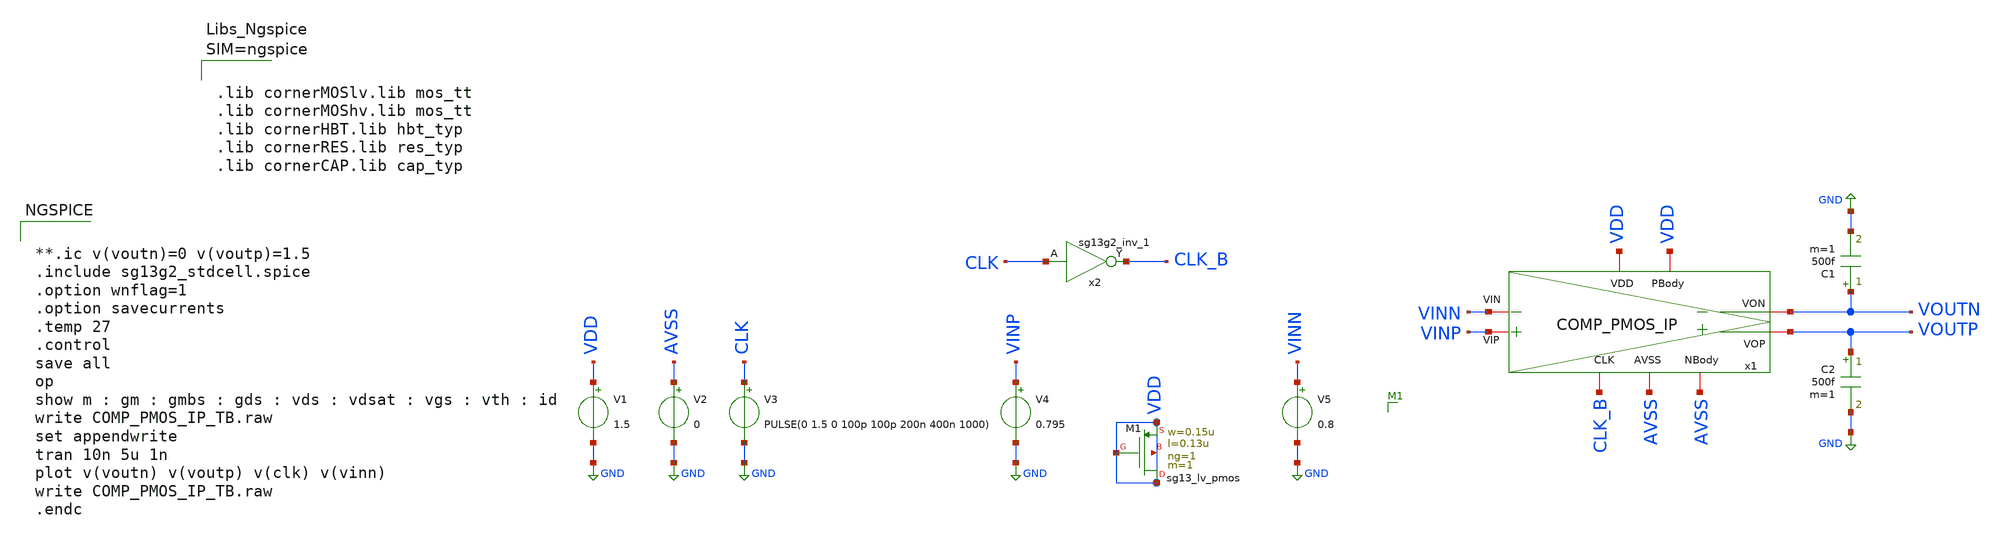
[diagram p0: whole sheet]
** sch_path: COMP/COMP_PMOS_IP_TB.sch
**.subckt COMP_PMOS_IP_TB
V1 VDD GND 1.5
V2 AVSS GND 0
V3 CLK GND PULSE(0 1.5 0 100p 100p 200n 400n 1000)
V4 VINP GND 0.795
V5 VINN GND 0.8
C1 VOUTN GND 500f m=1
C2 VOUTP GND 500f m=1
XM1 VDD VDD VDD VDD sg13_lv_pmos w=0.15u l=0.13u ng=1 m=1 mm_ok=1
x1 VDD CLK_B VDD VOUTN VOUTP VINP VINN AVSS AVSS COMP_PMOS_IP
x2 CLK_B CLK VDD AVSS sg13g2_inv_1
**** begin user architecture code


**.ic v(voutn)=0 v(voutp)=1.5
.include sg13g2_stdcell.spice
.option wnflag=1
.option savecurrents
.temp 27
.control
save all
op
show m : gm : gmbs : gds : vds : vdsat : vgs : vth : id
write COMP_PMOS_IP_TB.raw
set appendwrite
tran 10n 5u 1n
plot v(voutn) v(voutp) v(clk) v(vinn)
write COMP_PMOS_IP_TB.raw
.endc





.lib cornerMOSlv.lib mos_tt
.lib cornerMOShv.lib mos_tt
.lib cornerHBT.lib hbt_typ
.lib cornerRES.lib res_typ
.lib cornerCAP.lib cap_typ






.save @n.xm1.nsg13_lv_pmos[ids]
.save @n.xm1.nsg13_lv_pmos[gm]
.save @n.xm1.nsg13_lv_pmos[gds]
.save @n.xm1.nsg13_lv_pmos[vth]
.save @n.xm1.nsg13_lv_pmos[vgs]
.save @n.xm1.nsg13_lv_pmos[vdss]
.save @n.xm1.nsg13_lv_pmos[vds]
.save @n.xm1.nsg13_lv_pmos[cgg]
.save @n.xm1.nsg13_lv_pmos[cgsol]
.save @n.xm1.nsg13_lv_pmos[cgdol]
.save @n.x1.xmp_vip.nsg13_lv_pmos[ids]
.save @n.x1.xmp_vip.nsg13_lv_pmos[gm]
.save @n.x1.xmp_vip.nsg13_lv_pmos[gds]
.save @n.x1.xmp_vip.nsg13_lv_pmos[vth]
.save @n.x1.xmp_vip.nsg13_lv_pmos[vgs]
.save @n.x1.xmp_vip.nsg13_lv_pmos[vdss]
.save @n.x1.xmp_vip.nsg13_lv_pmos[vds]
.save @n.x1.xmp_vip.nsg13_lv_pmos[cgg]
.save @n.x1.xmp_vip.nsg13_lv_pmos[cgsol]
.save @n.x1.xmp_vip.nsg13_lv_pmos[cgdol]
.save @n.x1.xmp_vin.nsg13_lv_pmos[ids]
.save @n.x1.xmp_vin.nsg13_lv_pmos[gm]
.save @n.x1.xmp_vin.nsg13_lv_pmos[gds]
.save @n.x1.xmp_vin.nsg13_lv_pmos[vth]
.save @n.x1.xmp_vin.nsg13_lv_pmos[vgs]
.save @n.x1.xmp_vin.nsg13_lv_pmos[vdss]
.save @n.x1.xmp_vin.nsg13_lv_pmos[vds]
.save @n.x1.xmp_vin.nsg13_lv_pmos[cgg]
.save @n.x1.xmp_vin.nsg13_lv_pmos[cgsol]
.save @n.x1.xmp_vin.nsg13_lv_pmos[cgdol]
.save @n.x1.xmp_crs_cp1.nsg13_lv_pmos[ids]
.save @n.x1.xmp_crs_cp1.nsg13_lv_pmos[gm]
.save @n.x1.xmp_crs_cp1.nsg13_lv_pmos[gds]
.save @n.x1.xmp_crs_cp1.nsg13_lv_pmos[vth]
.save @n.x1.xmp_crs_cp1.nsg13_lv_pmos[vgs]
.save @n.x1.xmp_crs_cp1.nsg13_lv_pmos[vdss]
.save @n.x1.xmp_crs_cp1.nsg13_lv_pmos[vds]
.save @n.x1.xmp_crs_cp1.nsg13_lv_pmos[cgg]
.save @n.x1.xmp_crs_cp1.nsg13_lv_pmos[cgsol]
.save @n.x1.xmp_crs_cp1.nsg13_lv_pmos[cgdol]
.save @n.x1.xmp_crs_cp2.nsg13_lv_pmos[ids]
.save @n.x1.xmp_crs_cp2.nsg13_lv_pmos[gm]
.save @n.x1.xmp_crs_cp2.nsg13_lv_pmos[gds]
.save @n.x1.xmp_crs_cp2.nsg13_lv_pmos[vth]
.save @n.x1.xmp_crs_cp2.nsg13_lv_pmos[vgs]
.save @n.x1.xmp_crs_cp2.nsg13_lv_pmos[vdss]
.save @n.x1.xmp_crs_cp2.nsg13_lv_pmos[vds]
.save @n.x1.xmp_crs_cp2.nsg13_lv_pmos[cgg]
.save @n.x1.xmp_crs_cp2.nsg13_lv_pmos[cgsol]
.save @n.x1.xmp_crs_cp2.nsg13_lv_pmos[cgdol]
.save @n.x1.xm5.nsg13_lv_pmos[ids]
.save @n.x1.xm5.nsg13_lv_pmos[gm]
.save @n.x1.xm5.nsg13_lv_pmos[gds]
.save @n.x1.xm5.nsg13_lv_pmos[vth]
.save @n.x1.xm5.nsg13_lv_pmos[vgs]
.save @n.x1.xm5.nsg13_lv_pmos[vdss]
.save @n.x1.xm5.nsg13_lv_pmos[vds]
.save @n.x1.xm5.nsg13_lv_pmos[cgg]
.save @n.x1.xm5.nsg13_lv_pmos[cgsol]
.save @n.x1.xm5.nsg13_lv_pmos[cgdol]
.save @n.x1.xmn_crs_cp2.nsg13_lv_nmos[ids]
.save @n.x1.xmn_crs_cp2.nsg13_lv_nmos[gm]
.save @n.x1.xmn_crs_cp2.nsg13_lv_nmos[gds]
.save @n.x1.xmn_crs_cp2.nsg13_lv_nmos[vth]
.save @n.x1.xmn_crs_cp2.nsg13_lv_nmos[vgs]
.save @n.x1.xmn_crs_cp2.nsg13_lv_nmos[vdss]
.save @n.x1.xmn_crs_cp2.nsg13_lv_nmos[vds]
.save @n.x1.xmn_crs_cp2.nsg13_lv_nmos[cgg]
.save @n.x1.xmn_crs_cp2.nsg13_lv_nmos[cgsol]
.save @n.x1.xmn_crs_cp2.nsg13_lv_nmos[cgdol]
.save @n.x1.xmn_crs_cp1.nsg13_lv_nmos[ids]
.save @n.x1.xmn_crs_cp1.nsg13_lv_nmos[gm]
.save @n.x1.xmn_crs_cp1.nsg13_lv_nmos[gds]
.save @n.x1.xmn_crs_cp1.nsg13_lv_nmos[vth]
.save @n.x1.xmn_crs_cp1.nsg13_lv_nmos[vgs]
.save @n.x1.xmn_crs_cp1.nsg13_lv_nmos[vdss]
.save @n.x1.xmn_crs_cp1.nsg13_lv_nmos[vds]
.save @n.x1.xmn_crs_cp1.nsg13_lv_nmos[cgg]
.save @n.x1.xmn_crs_cp1.nsg13_lv_nmos[cgsol]
.save @n.x1.xmn_crs_cp1.nsg13_lv_nmos[cgdol]
.save @n.x1.xmn_pc_out_p.nsg13_lv_nmos[ids]
.save @n.x1.xmn_pc_out_p.nsg13_lv_nmos[gm]
.save @n.x1.xmn_pc_out_p.nsg13_lv_nmos[gds]
.save @n.x1.xmn_pc_out_p.nsg13_lv_nmos[vth]
.save @n.x1.xmn_pc_out_p.nsg13_lv_nmos[vgs]
.save @n.x1.xmn_pc_out_p.nsg13_lv_nmos[vdss]
.save @n.x1.xmn_pc_out_p.nsg13_lv_nmos[vds]
.save @n.x1.xmn_pc_out_p.nsg13_lv_nmos[cgg]
.save @n.x1.xmn_pc_out_p.nsg13_lv_nmos[cgsol]
.save @n.x1.xmn_pc_out_p.nsg13_lv_nmos[cgdol]
.save @n.x1.xmn_pc_out_n.nsg13_lv_nmos[ids]
.save @n.x1.xmn_pc_out_n.nsg13_lv_nmos[gm]
.save @n.x1.xmn_pc_out_n.nsg13_lv_nmos[gds]
.save @n.x1.xmn_pc_out_n.nsg13_lv_nmos[vth]
.save @n.x1.xmn_pc_out_n.nsg13_lv_nmos[vgs]
.save @n.x1.xmn_pc_out_n.nsg13_lv_nmos[vdss]
.save @n.x1.xmn_pc_out_n.nsg13_lv_nmos[vds]
.save @n.x1.xmn_pc_out_n.nsg13_lv_nmos[cgg]
.save @n.x1.xmn_pc_out_n.nsg13_lv_nmos[cgsol]
.save @n.x1.xmn_pc_out_n.nsg13_lv_nmos[cgdol]
.save @n.x1.xmn_pc_ip_p.nsg13_lv_nmos[ids]
.save @n.x1.xmn_pc_ip_p.nsg13_lv_nmos[gm]
.save @n.x1.xmn_pc_ip_p.nsg13_lv_nmos[gds]
.save @n.x1.xmn_pc_ip_p.nsg13_lv_nmos[vth]
.save @n.x1.xmn_pc_ip_p.nsg13_lv_nmos[vgs]
.save @n.x1.xmn_pc_ip_p.nsg13_lv_nmos[vdss]
.save @n.x1.xmn_pc_ip_p.nsg13_lv_nmos[vds]
.save @n.x1.xmn_pc_ip_p.nsg13_lv_nmos[cgg]
.save @n.x1.xmn_pc_ip_p.nsg13_lv_nmos[cgsol]
.save @n.x1.xmn_pc_ip_p.nsg13_lv_nmos[cgdol]
.save @n.x1.xmn_pc_ip_n.nsg13_lv_nmos[ids]
.save @n.x1.xmn_pc_ip_n.nsg13_lv_nmos[gm]
.save @n.x1.xmn_pc_ip_n.nsg13_lv_nmos[gds]
.save @n.x1.xmn_pc_ip_n.nsg13_lv_nmos[vth]
.save @n.x1.xmn_pc_ip_n.nsg13_lv_nmos[vgs]
.save @n.x1.xmn_pc_ip_n.nsg13_lv_nmos[vdss]
.save @n.x1.xmn_pc_ip_n.nsg13_lv_nmos[vds]
.save @n.x1.xmn_pc_ip_n.nsg13_lv_nmos[cgg]
.save @n.x1.xmn_pc_ip_n.nsg13_lv_nmos[cgsol]
.save @n.x1.xmn_pc_ip_n.nsg13_lv_nmos[cgdol]
.save @n.x1.xm12.nsg13_lv_nmos[ids]
.save @n.x1.xm12.nsg13_lv_nmos[gm]
.save @n.x1.xm12.nsg13_lv_nmos[gds]
.save @n.x1.xm12.nsg13_lv_nmos[vth]
.save @n.x1.xm12.nsg13_lv_nmos[vgs]
.save @n.x1.xm12.nsg13_lv_nmos[vdss]
.save @n.x1.xm12.nsg13_lv_nmos[vds]
.save @n.x1.xm12.nsg13_lv_nmos[cgg]
.save @n.x1.xm12.nsg13_lv_nmos[cgsol]
.save @n.x1.xm12.nsg13_lv_nmos[cgdol]
.save @n.x1.xm13.nsg13_lv_pmos[ids]
.save @n.x1.xm13.nsg13_lv_pmos[gm]
.save @n.x1.xm13.nsg13_lv_pmos[gds]
.save @n.x1.xm13.nsg13_lv_pmos[vth]
.save @n.x1.xm13.nsg13_lv_pmos[vgs]
.save @n.x1.xm13.nsg13_lv_pmos[vdss]
.save @n.x1.xm13.nsg13_lv_pmos[vds]
.save @n.x1.xm13.nsg13_lv_pmos[cgg]
.save @n.x1.xm13.nsg13_lv_pmos[cgsol]
.save @n.x1.xm13.nsg13_lv_pmos[cgdol]
.save @n.x1.xm14.nsg13_lv_nmos[ids]
.save @n.x1.xm14.nsg13_lv_nmos[gm]
.save @n.x1.xm14.nsg13_lv_nmos[gds]
.save @n.x1.xm14.nsg13_lv_nmos[vth]
.save @n.x1.xm14.nsg13_lv_nmos[vgs]
.save @n.x1.xm14.nsg13_lv_nmos[vdss]
.save @n.x1.xm14.nsg13_lv_nmos[vds]
.save @n.x1.xm14.nsg13_lv_nmos[cgg]
.save @n.x1.xm14.nsg13_lv_nmos[cgsol]
.save @n.x1.xm14.nsg13_lv_nmos[cgdol]
.save @n.x1.xm15.nsg13_lv_pmos[ids]
.save @n.x1.xm15.nsg13_lv_pmos[gm]
.save @n.x1.xm15.nsg13_lv_pmos[gds]
.save @n.x1.xm15.nsg13_lv_pmos[vth]
.save @n.x1.xm15.nsg13_lv_pmos[vgs]
.save @n.x1.xm15.nsg13_lv_pmos[vdss]
.save @n.x1.xm15.nsg13_lv_pmos[vds]
.save @n.x1.xm15.nsg13_lv_pmos[cgg]
.save @n.x1.xm15.nsg13_lv_pmos[cgsol]
.save @n.x1.xm15.nsg13_lv_pmos[cgdol]


**** end user architecture code
**.ends

* expanding   symbol:  /foss/designs/SAR_ADC_8_Bit_IHP130/COMP/COMP_PMOS_IP.sym # of pins=9
** sym_path: COMP/COMP_PMOS_IP.sym
** sch_path: COMP/COMP_PMOS_IP.sch
.subckt COMP_PMOS_IP VDD CLK PBody VON VOP VIP VIN NBody AVSS
*.iopin VDD
*.iopin CLK
*.iopin PBody
*.iopin VON
*.iopin VOP
*.iopin VIP
*.iopin VIN
*.iopin NBody
*.iopin AVSS
XMP_VIP net4 VIP net1 PBody sg13_lv_pmos w=3u l=0.13u ng=1 m=8 mm_ok=1
XMP_VIN net5 VIN net1 PBody sg13_lv_pmos w=3u l=0.13u ng=1 m=8 mm_ok=1
XMP_CRS_CP1 net3 net2 net4 PBody sg13_lv_pmos w=1u l=0.13u ng=1 m=8 mm_ok=1
XMP_CRS_CP2 net2 net3 net5 PBody sg13_lv_pmos w=1u l=0.13u ng=1 m=8 mm_ok=1
XM5 net1 CLK VDD PBody sg13_lv_pmos w=1u l=0.13u ng=1 m=8 mm_ok=1
XMN_CRS_CP2 net2 net3 AVSS NBody sg13_lv_nmos w=0.15u l=0.13u ng=1 m=1 mm_ok=1
XMN_CRS_CP1 net3 net2 AVSS NBody sg13_lv_nmos w=0.15u l=0.13u ng=1 m=1 mm_ok=1
XMN_PC_OUT_P net4 CLK AVSS NBody sg13_lv_nmos w=0.15u l=0.13u ng=1 m=1 mm_ok=1
XMN_PC_OUT_N net5 CLK AVSS NBody sg13_lv_nmos w=0.15u l=0.13u ng=1 m=1 mm_ok=1
XMN_PC_IP_P net3 CLK AVSS NBody sg13_lv_nmos w=0.15u l=0.13u ng=1 m=1 mm_ok=1
XMN_PC_IP_N net2 CLK AVSS NBody sg13_lv_nmos w=0.15u l=0.13u ng=1 m=1 mm_ok=1
.save v(vip)
.save v(vin)
XM12 VOP net3 AVSS NBody sg13_lv_nmos w=0.15u l=0.13u ng=1 m=1 mm_ok=1
XM13 VOP net3 VDD PBody sg13_lv_pmos w=1u l=0.13u ng=1 m=1 mm_ok=1
XM14 VON net2 AVSS NBody sg13_lv_nmos w=0.15u l=0.13u ng=1 m=1 mm_ok=1
XM15 VON net2 VDD PBody sg13_lv_pmos w=1u l=0.13u ng=1 m=1 mm_ok=1
.save v(net1)
.save v(net5)
.save v(net4)
.save v(net3)
.save v(net2)
.ends


* expanding   symbol:  sg13g2_stdcells/sg13g2_inv_1.sym # of pins=2
** sym_path: sg13g2_stdcells/sg13g2_inv_1.sym
** sch_path: sg13g2_stdcells/sg13g2_inv_1.sch
.subckt sg13g2_inv_1 Y A VDD VSS
*.opin Y
*.ipin A
*.iopin VDD
*.iopin VSS
XM1 Y A VSS VSS sg13_lv_nmos w=740.00n l=130.00n ng=1 m=1 mm_ok=1
XM2 Y A VDD VDD sg13_lv_pmos w=1.12u l=130.00n ng=1 m=1 mm_ok=1
.ends

.GLOBAL GND
.end
